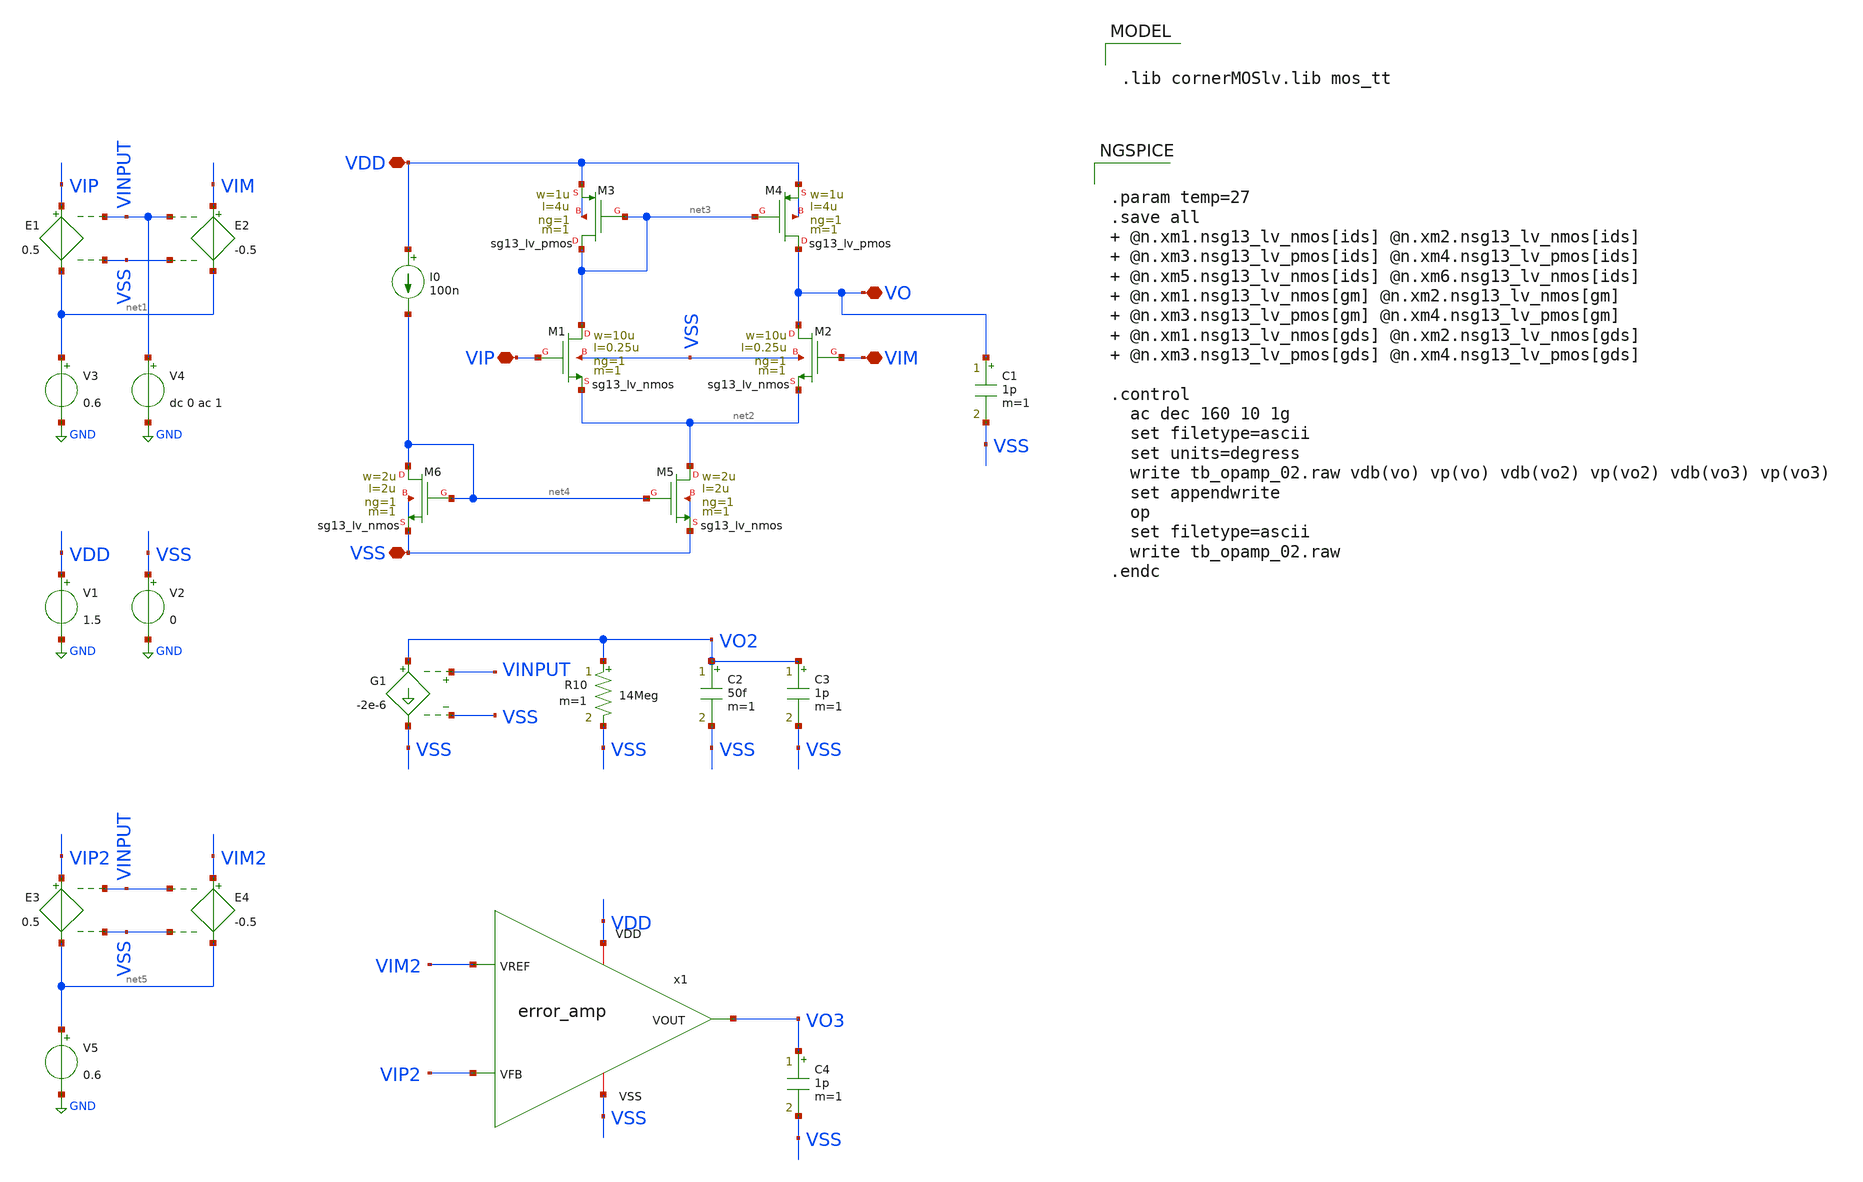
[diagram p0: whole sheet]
** sch_path: analog/tb/tb_opamp_01.sch
**.subckt tb_opamp_01 VIM VIP VSS VDD VO
*.iopin VIM
*.iopin VIP
*.iopin VSS
*.iopin VDD
*.iopin VO
C1 VO VSS 1p m=1
V1 VDD GND 1.5
E1 VIP net1 VINPUT VSS 0.5
V2 VSS GND 0
E2 VIM net1 VINPUT VSS -0.5
V3 net1 GND 0.6
V4 VINPUT GND dc 0 ac 1
XM1 net3 VIP net2 VSS sg13_lv_nmos w=10u l=0.25u ng=1 m=1 mm_ok=1
XM2 VO VIM net2 VSS sg13_lv_nmos w=10u l=0.25u ng=1 m=1 mm_ok=1
XM3 net3 net3 VDD VDD sg13_lv_pmos w=1u l=4u ng=1 m=1 mm_ok=1
XM4 VO net3 VDD VDD sg13_lv_pmos w=1u l=4u ng=1 m=1 mm_ok=1
XM5 net2 net4 VSS VSS sg13_lv_nmos w=2u l=2u ng=1 m=1 mm_ok=1
XM6 net4 net4 VSS VSS sg13_lv_nmos w=2u l=2u ng=1 m=1 mm_ok=1
I0 VDD net4 100n
R10 VO2 VSS 14Meg m=1
C2 VO2 VSS 50f m=1
C3 VO2 VSS 1p m=1
G1 VO2 VSS VINPUT VSS -2e-6
x1 VDD VO3 VIM2 VIP2 VSS error_amp
C4 VO3 VSS 1p m=1
E3 VIP2 net5 VINPUT VSS 0.5
E4 VIM2 net5 VINPUT VSS -0.5
V5 net5 GND 0.6
**** begin user architecture code


.param temp=27
.save all  @n.xm1.nsg13_lv_nmos[ids] @n.xm2.nsg13_lv_nmos[ids]  @n.xm3.nsg13_lv_pmos[ids] @n.xm4.nsg13_lv_pmos[ids]  @n.xm5.nsg13_lv_nmos[ids] @n.xm6.nsg13_lv_nmos[ids]  @n.xm1.nsg13_lv_nmos[gm] @n.xm2.nsg13_lv_nmos[gm]  @n.xm3.nsg13_lv_pmos[gm] @n.xm4.nsg13_lv_pmos[gm]  @n.xm1.nsg13_lv_nmos[gds] @n.xm2.nsg13_lv_nmos[gds]  @n.xm3.nsg13_lv_pmos[gds] @n.xm4.nsg13_lv_pmos[gds]

.control
  ac dec 160 10 1g
  set filetype=ascii
  set units=degress
  write tb_opamp_02.raw vdb(vo) vp(vo) vdb(vo2) vp(vo2) vdb(vo3) vp(vo3)
  set appendwrite
  op
  set filetype=ascii
  write tb_opamp_02.raw
.endc




.lib cornerMOSlv.lib mos_tt


**** end user architecture code
**.ends

* expanding   symbol:  error_amp.sym # of pins=5
** sym_path: analog/core/error_amp.sym
** sch_path: analog/core/error_amp.sch
.subckt error_amp VDD VOUT VREF VFB VSS
*.ipin VREF
*.iopin VDD
*.opin VOUT
*.ipin VFB
*.iopin VSS
XMldo1 net1 VFB net2 VSS sg13_lv_nmos w=1.2u l=0.13u ng=1 m=1 mm_ok=1
XMldo4 VOUT net1 VDD VDD sg13_lv_pmos w=2.4u l=0.13u ng=1 m=1 mm_ok=1
XMldo2 VOUT VREF net2 VSS sg13_lv_nmos w=1.2u l=0.13u ng=1 m=1 mm_ok=1
XMldo3 net1 net1 VDD VDD sg13_lv_pmos w=2.4u l=0.13u ng=1 m=1 mm_ok=1
XMldo5 net2 net3 VSS VSS sg13_lv_nmos w=2u l=0.13u ng=1 m=1 mm_ok=1
XMldo6 net3 net3 VSS VSS sg13_lv_nmos w=1u l=0.13u ng=1 m=1 mm_ok=1
I0 VDD net3 2u
.ends

.GLOBAL GND
.end
